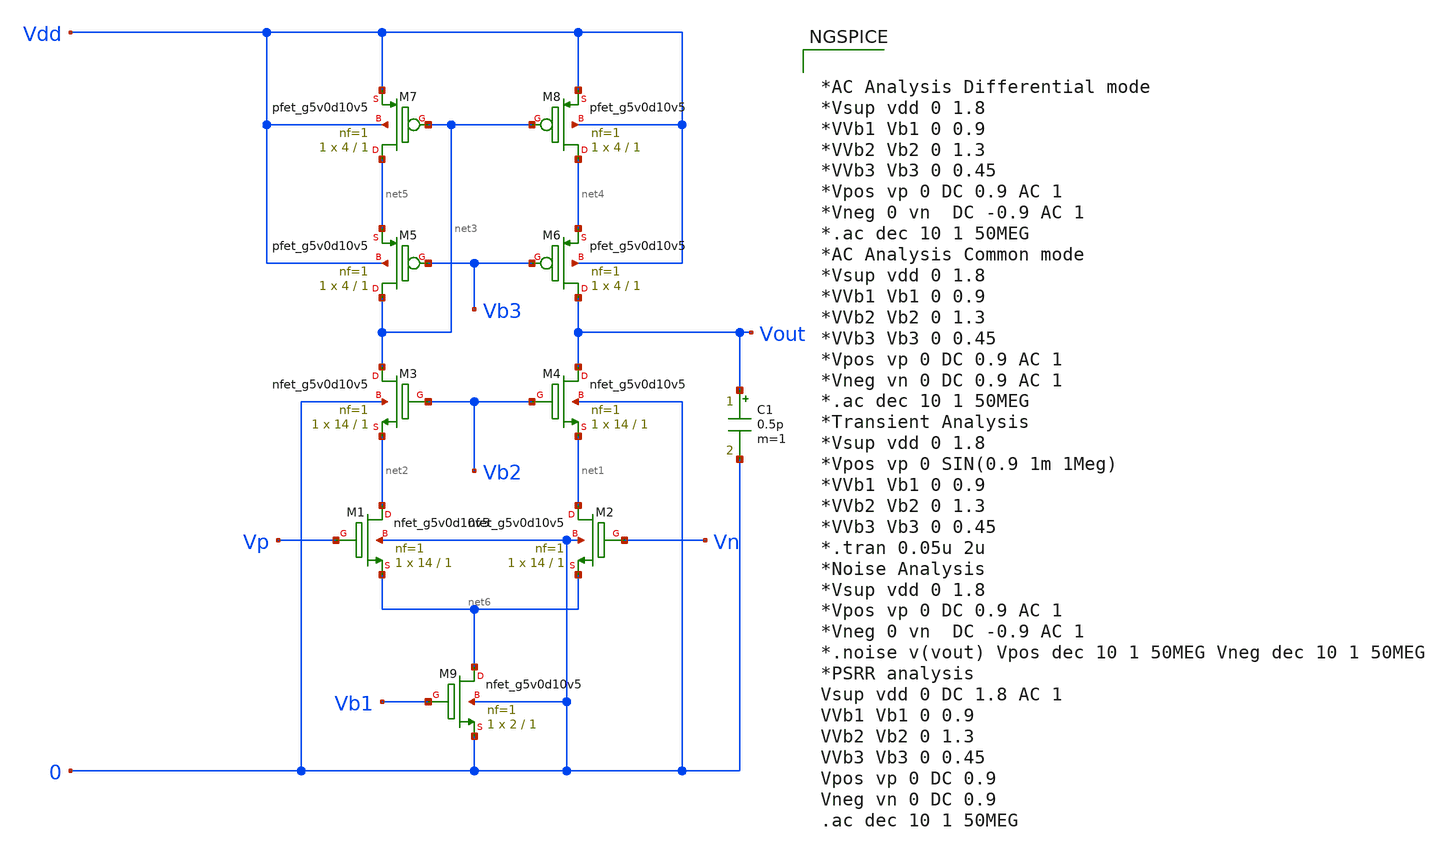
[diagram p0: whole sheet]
** sch_path: OTA/Schematic/Telescopic_OTA.sch
**.subckt Telescopic_OTA
C1 Vout 0 0.5p m=1
XM9 net6 Vb1 0 0 sky130_fd_pr__nfet_g5v0d10v5 L=1 W=2 nf=1 ad='int((nf+1)/2) * W/nf * 0.29' as='int((nf+2)/2) * W/nf * 0.29'
+ pd='2*int((nf+1)/2) * (W/nf + 0.29)' ps='2*int((nf+2)/2) * (W/nf + 0.29)' nrd='0.29 / W' nrs='0.29 / W'
+ sa=0 sb=0 sd=0 mult=1 m=1
XM1 net2 Vp net6 0 sky130_fd_pr__nfet_g5v0d10v5 L=1 W=14 nf=1 ad='int((nf+1)/2) * W/nf * 0.29' as='int((nf+2)/2) * W/nf * 0.29'
+ pd='2*int((nf+1)/2) * (W/nf + 0.29)' ps='2*int((nf+2)/2) * (W/nf + 0.29)' nrd='0.29 / W' nrs='0.29 / W'
+ sa=0 sb=0 sd=0 mult=1 m=1
XM2 net1 Vn net6 0 sky130_fd_pr__nfet_g5v0d10v5 L=1 W=14 nf=1 ad='int((nf+1)/2) * W/nf * 0.29' as='int((nf+2)/2) * W/nf * 0.29'
+ pd='2*int((nf+1)/2) * (W/nf + 0.29)' ps='2*int((nf+2)/2) * (W/nf + 0.29)' nrd='0.29 / W' nrs='0.29 / W'
+ sa=0 sb=0 sd=0 mult=1 m=1
XM3 net3 Vb2 net2 0 sky130_fd_pr__nfet_g5v0d10v5 L=1 W=14 nf=1 ad='int((nf+1)/2) * W/nf * 0.29' as='int((nf+2)/2) * W/nf * 0.29'
+ pd='2*int((nf+1)/2) * (W/nf + 0.29)' ps='2*int((nf+2)/2) * (W/nf + 0.29)' nrd='0.29 / W' nrs='0.29 / W'
+ sa=0 sb=0 sd=0 mult=1 m=1
XM4 Vout Vb2 net1 0 sky130_fd_pr__nfet_g5v0d10v5 L=1 W=14 nf=1 ad='int((nf+1)/2) * W/nf * 0.29' as='int((nf+2)/2) * W/nf * 0.29'
+ pd='2*int((nf+1)/2) * (W/nf + 0.29)' ps='2*int((nf+2)/2) * (W/nf + 0.29)' nrd='0.29 / W' nrs='0.29 / W'
+ sa=0 sb=0 sd=0 mult=1 m=1
XM5 net3 Vb3 net5 Vdd sky130_fd_pr__pfet_g5v0d10v5 L=1 W=4 nf=1 ad='int((nf+1)/2) * W/nf * 0.29' as='int((nf+2)/2) * W/nf * 0.29'
+ pd='2*int((nf+1)/2) * (W/nf + 0.29)' ps='2*int((nf+2)/2) * (W/nf + 0.29)' nrd='0.29 / W' nrs='0.29 / W'
+ sa=0 sb=0 sd=0 mult=1 m=1
XM6 Vout Vb3 net4 Vdd sky130_fd_pr__pfet_g5v0d10v5 L=1 W=4 nf=1 ad='int((nf+1)/2) * W/nf * 0.29' as='int((nf+2)/2) * W/nf * 0.29'
+ pd='2*int((nf+1)/2) * (W/nf + 0.29)' ps='2*int((nf+2)/2) * (W/nf + 0.29)' nrd='0.29 / W' nrs='0.29 / W'
+ sa=0 sb=0 sd=0 mult=1 m=1
XM7 net5 net3 Vdd Vdd sky130_fd_pr__pfet_g5v0d10v5 L=1 W=4 nf=1 ad='int((nf+1)/2) * W/nf * 0.29' as='int((nf+2)/2) * W/nf * 0.29'
+ pd='2*int((nf+1)/2) * (W/nf + 0.29)' ps='2*int((nf+2)/2) * (W/nf + 0.29)' nrd='0.29 / W' nrs='0.29 / W'
+ sa=0 sb=0 sd=0 mult=1 m=1
XM8 net4 net3 Vdd Vdd sky130_fd_pr__pfet_g5v0d10v5 L=1 W=4 nf=1 ad='int((nf+1)/2) * W/nf * 0.29' as='int((nf+2)/2) * W/nf * 0.29'
+ pd='2*int((nf+1)/2) * (W/nf + 0.29)' ps='2*int((nf+2)/2) * (W/nf + 0.29)' nrd='0.29 / W' nrs='0.29 / W'
+ sa=0 sb=0 sd=0 mult=1 m=1
**** begin user architecture code


*AC Analysis Differential mode
*Vsup vdd 0 1.8
*VVb1 Vb1 0 0.9
*VVb2 Vb2 0 1.3
*VVb3 Vb3 0 0.45
*Vpos vp 0 DC 0.9 AC 1
*Vneg 0 vn  DC -0.9 AC 1
*.ac dec 10 1 50MEG
*AC Analysis Common mode
*Vsup vdd 0 1.8
*VVb1 Vb1 0 0.9
*VVb2 Vb2 0 1.3
*VVb3 Vb3 0 0.45
*Vpos vp 0 DC 0.9 AC 1
*Vneg vn 0 DC 0.9 AC 1
*.ac dec 10 1 50MEG
*Transient Analysis
*Vsup vdd 0 1.8
*Vpos vp 0 SIN(0.9 1m 1Meg)
*VVb1 Vb1 0 0.9
*VVb2 Vb2 0 1.3
*VVb3 Vb3 0 0.45
*.tran 0.05u 2u
*Noise Analysis
*Vsup vdd 0 1.8
*Vpos vp 0 DC 0.9 AC 1
*Vneg 0 vn  DC -0.9 AC 1
*.noise v(vout) Vpos dec 10 1 50MEG Vneg dec 10 1 50MEG
*PSRR analysis
Vsup vdd 0 DC 1.8 AC 1
VVb1 Vb1 0 0.9
VVb2 Vb2 0 1.3
VVb3 Vb3 0 0.45
Vpos vp 0 DC 0.9
Vneg vn 0 DC 0.9
.ac dec 10 1 50MEG



.include $::SKYWATER_MODELS/cells/nfet_01v8/sky130_fd_pr__nfet_01v8__tt.corner.spice
.include $::SKYWATER_MODELS/cells/nfet_01v8_lvt/sky130_fd_pr__nfet_01v8_lvt__tt.corner.spice
.include $::SKYWATER_MODELS/cells/pfet_01v8/sky130_fd_pr__pfet_01v8__tt.corner.spice
.include $::SKYWATER_MODELS/cells/nfet_03v3_nvt/sky130_fd_pr__nfet_03v3_nvt__tt.corner.spice
.include $::SKYWATER_MODELS/cells/nfet_05v0_nvt/sky130_fd_pr__nfet_05v0_nvt__tt.corner.spice
.include $::SKYWATER_MODELS/cells/esd_nfet_01v8/sky130_fd_pr__esd_nfet_01v8__tt.corner.spice
.include $::SKYWATER_MODELS/cells/pfet_01v8_lvt/sky130_fd_pr__pfet_01v8_lvt__tt.corner.spice
.include $::SKYWATER_MODELS/cells/pfet_01v8_hvt/sky130_fd_pr__pfet_01v8_hvt__tt.corner.spice
.include $::SKYWATER_MODELS/cells/esd_pfet_g5v0d10v5/sky130_fd_pr__esd_pfet_g5v0d10v5__tt.corner.spice
.include $::SKYWATER_MODELS/cells/pfet_g5v0d10v5/sky130_fd_pr__pfet_g5v0d10v5__tt.corner.spice
.include $::SKYWATER_MODELS/cells/pfet_g5v0d16v0/sky130_fd_pr__pfet_g5v0d16v0__tt.corner.spice
.include $::SKYWATER_MODELS/cells/nfet_g5v0d10v5/sky130_fd_pr__nfet_g5v0d10v5__tt.corner.spice
.include $::SKYWATER_MODELS/cells/nfet_g5v0d16v0/sky130_fd_pr__nfet_g5v0d16v0__tt_discrete.corner.spice
.include $::SKYWATER_MODELS/cells/esd_nfet_g5v0d10v5/sky130_fd_pr__esd_nfet_g5v0d10v5__tt.corner.spice
.include $::SKYWATER_MODELS/models/corners/tt/nonfet.spice
* Mismatch parameters
.include $::SKYWATER_MODELS/cells/nfet_01v8/sky130_fd_pr__nfet_01v8__mismatch.corner.spice
.include $::SKYWATER_MODELS/cells/pfet_01v8/sky130_fd_pr__pfet_01v8__mismatch.corner.spice
.include $::SKYWATER_MODELS/cells/nfet_01v8_lvt/sky130_fd_pr__nfet_01v8_lvt__mismatch.corner.spice
.include $::SKYWATER_MODELS/cells/pfet_01v8_lvt/sky130_fd_pr__pfet_01v8_lvt__mismatch.corner.spice
.include $::SKYWATER_MODELS/cells/pfet_01v8_hvt/sky130_fd_pr__pfet_01v8_hvt__mismatch.corner.spice
.include $::SKYWATER_MODELS/cells/nfet_g5v0d10v5/sky130_fd_pr__nfet_g5v0d10v5__mismatch.corner.spice
.include $::SKYWATER_MODELS/cells/pfet_g5v0d10v5/sky130_fd_pr__pfet_g5v0d10v5__mismatch.corner.spice
.include $::SKYWATER_MODELS/cells/nfet_05v0_nvt/sky130_fd_pr__nfet_05v0_nvt__mismatch.corner.spice
.include $::SKYWATER_MODELS/cells/nfet_03v3_nvt/sky130_fd_pr__nfet_03v3_nvt__mismatch.corner.spice
* Resistor$::SKYWATER_MODELS/Capacitor
.include $::SKYWATER_MODELS/models/r+c/res_typical__cap_typical.spice
.include $::SKYWATER_MODELS/models/r+c/res_typical__cap_typical__lin.spice
* Special cells
.include $::SKYWATER_MODELS/models/corners/tt/specialized_cells.spice
* All models
.include $::SKYWATER_MODELS/models/all.spice
* Corner
.include $::SKYWATER_MODELS/models/corners/tt/rf.spice

**** end user architecture code
**.ends
.end
